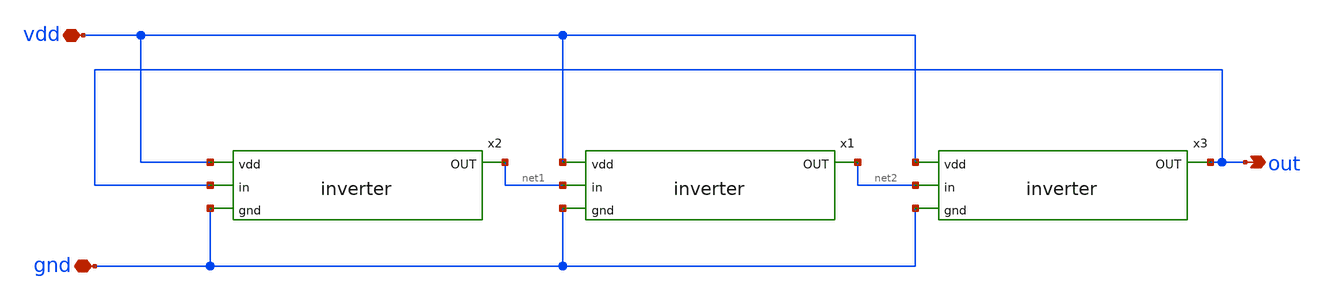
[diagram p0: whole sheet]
** sch_path: oscillator.sch
**.subckt oscillator out vdd gnd
*.opin out
*.iopin vdd
*.iopin gnd
x1 vdd net1 net2 gnd inverter
x2 vdd out net1 gnd inverter
x3 vdd net2 out gnd inverter
**.ends

* expanding   symbol:  inverter.sym # of pins=4
** sym_path: inverter.sym
** sch_path: inverter.sch
.subckt inverter vdd in OUT gnd
*.ipin vdd
*.ipin in
*.ipin gnd
*.opin OUT
XM1 OUT in gnd gnd sky130_fd_pr__nfet_01v8 L=0.15 W=1 nf=1 ad='int((nf+1)/2) * W/nf * 0.29' as='int((nf+2)/2) * W/nf * 0.29'
+ pd='2*int((nf+1)/2) * (W/nf + 0.29)' ps='2*int((nf+2)/2) * (W/nf + 0.29)' nrd='0.29 / W' nrs='0.29 / W'
+ sa=0 sb=0 sd=0 mult=1 m=1
XM2 OUT in vdd vdd sky130_fd_pr__pfet_01v8 L=0.15 W=1 nf=1 ad='int((nf+1)/2) * W/nf * 0.29' as='int((nf+2)/2) * W/nf * 0.29'
+ pd='2*int((nf+1)/2) * (W/nf + 0.29)' ps='2*int((nf+2)/2) * (W/nf + 0.29)' nrd='0.29 / W' nrs='0.29 / W'
+ sa=0 sb=0 sd=0 mult=1 m=1
.ends

.end
